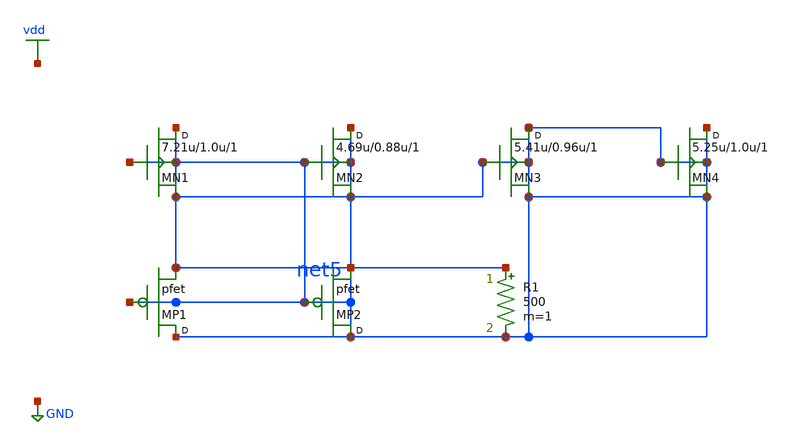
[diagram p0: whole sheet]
** sch_path: synthetic/generated/0024_synthetic.sch
**.subckt 0024_synthetic
MN1 net5 net5 net5 net5 nfet w=7.21u l=1.0u m=1
MN2 net5 net5 net5 net5 nfet w=4.69u l=0.88u m=1
MN3 net5 net5 net5 net5 nfet w=5.41u l=0.96u m=1
MN4 net5 net5 net5 net5 nfet w=5.25u l=1.0u m=1
MP1 net5 net5 net5 pfet m=1
MP2 net5 net5 net5 pfet m=1
R1 net5 net5 500 m=1
**.ends
.GLOBAL vdd
.GLOBAL GND
.end
